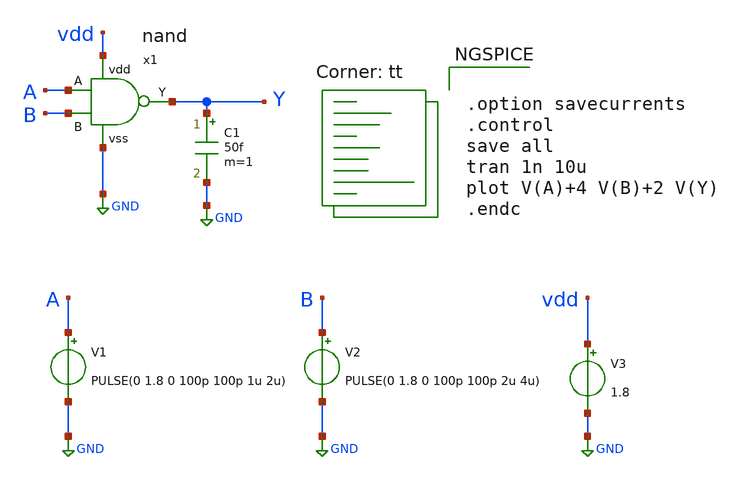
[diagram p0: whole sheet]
** sch_path: xschem/nand/nand_tb.sch
**.subckt nand_tb
x1 vdd GND A B Y nand
C1 Y GND 50f m=1
V1 A GND PULSE(0 1.8 0 100p 100p 1u 2u)
V2 B GND PULSE(0 1.8 0 100p 100p 2u 4u)
V3 vdd GND 1.8
**** begin user architecture code
.lib $::SKYWATER_MODELS/sky130.lib.spice tt


.option savecurrents
.control
save all
tran 1n 10u
plot V(A)+4 V(B)+2 V(Y)
.endc


**** end user architecture code
**.ends
.GLOBAL GND
.end
